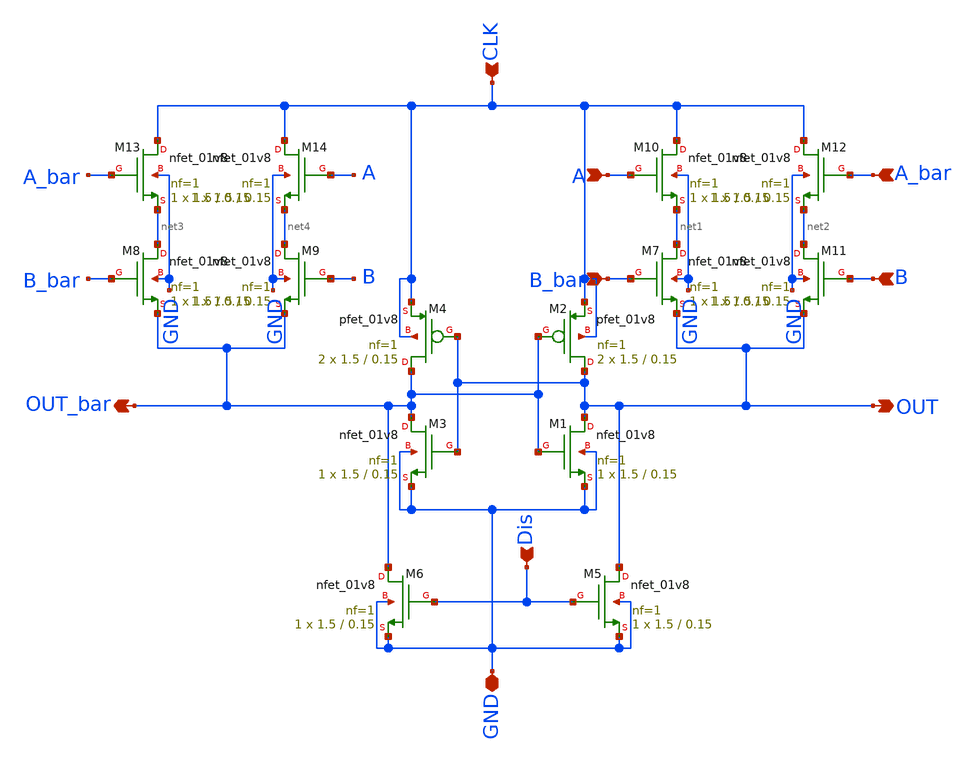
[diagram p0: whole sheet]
** sch_path: skywater_stuff/EESPFAL_XOR_v3_magic_checked.sch
**.subckt EESPFAL_XOR_v3_magic_checked A A_bar B B_bar OUT OUT_bar Dis GND CLK
*.ipin A
*.ipin A_bar
*.ipin B
*.ipin B_bar
*.opin OUT
*.opin OUT_bar
*.ipin Dis
*.iopin GND
*.ipin CLK
XM4 OUT_bar OUT CLK CLK sky130_fd_pr__pfet_01v8 L=0.15 W=1.5 nf=1 ad='int((nf+1)/2) * W/nf * 0.29' as='int((nf+2)/2) * W/nf * 0.29'
+ pd='2*int((nf+1)/2) * (W/nf + 0.29)' ps='2*int((nf+2)/2) * (W/nf + 0.29)' nrd='0.29 / W' nrs='0.29 / W'
+ sa=0 sb=0 sd=0 mult=2 m=2
XM3 OUT_bar OUT GND GND sky130_fd_pr__nfet_01v8 L=0.15 W=1.5 nf=1 ad='int((nf+1)/2) * W/nf * 0.29' as='int((nf+2)/2) * W/nf * 0.29'
+ pd='2*int((nf+1)/2) * (W/nf + 0.29)' ps='2*int((nf+2)/2) * (W/nf + 0.29)' nrd='0.29 / W' nrs='0.29 / W'
+ sa=0 sb=0 sd=0 mult=1 m=1
XM2 OUT OUT_bar CLK CLK sky130_fd_pr__pfet_01v8 L=0.15 W=1.5 nf=1 ad='int((nf+1)/2) * W/nf * 0.29' as='int((nf+2)/2) * W/nf * 0.29'
+ pd='2*int((nf+1)/2) * (W/nf + 0.29)' ps='2*int((nf+2)/2) * (W/nf + 0.29)' nrd='0.29 / W' nrs='0.29 / W'
+ sa=0 sb=0 sd=0 mult=2 m=2
XM11 net2 B OUT GND sky130_fd_pr__nfet_01v8 L=0.15 W=1.5 nf=1 ad='int((nf+1)/2) * W/nf * 0.29' as='int((nf+2)/2) * W/nf * 0.29'
+ pd='2*int((nf+1)/2) * (W/nf + 0.29)' ps='2*int((nf+2)/2) * (W/nf + 0.29)' nrd='0.29 / W' nrs='0.29 / W'
+ sa=0 sb=0 sd=0 mult=1 m=1
XM10 CLK A net1 GND sky130_fd_pr__nfet_01v8 L=0.15 W=1.5 nf=1 ad='int((nf+1)/2) * W/nf * 0.29' as='int((nf+2)/2) * W/nf * 0.29'
+ pd='2*int((nf+1)/2) * (W/nf + 0.29)' ps='2*int((nf+2)/2) * (W/nf + 0.29)' nrd='0.29 / W' nrs='0.29 / W'
+ sa=0 sb=0 sd=0 mult=1 m=1
XM12 CLK A_bar net2 GND sky130_fd_pr__nfet_01v8 L=0.15 W=1.5 nf=1 ad='int((nf+1)/2) * W/nf * 0.29' as='int((nf+2)/2) * W/nf * 0.29'
+ pd='2*int((nf+1)/2) * (W/nf + 0.29)' ps='2*int((nf+2)/2) * (W/nf + 0.29)' nrd='0.29 / W' nrs='0.29 / W'
+ sa=0 sb=0 sd=0 mult=1 m=1
XM8 net3 B_bar OUT_bar GND sky130_fd_pr__nfet_01v8 L=0.15 W=1.5 nf=1 ad='int((nf+1)/2) * W/nf * 0.29'
+ as='int((nf+2)/2) * W/nf * 0.29' pd='2*int((nf+1)/2) * (W/nf + 0.29)' ps='2*int((nf+2)/2) * (W/nf + 0.29)'
+ nrd='0.29 / W' nrs='0.29 / W' sa=0 sb=0 sd=0 mult=1 m=1
XM9 net4 B OUT_bar GND sky130_fd_pr__nfet_01v8 L=0.15 W=1.5 nf=1 ad='int((nf+1)/2) * W/nf * 0.29' as='int((nf+2)/2) * W/nf * 0.29'
+ pd='2*int((nf+1)/2) * (W/nf + 0.29)' ps='2*int((nf+2)/2) * (W/nf + 0.29)' nrd='0.29 / W' nrs='0.29 / W'
+ sa=0 sb=0 sd=0 mult=1 m=1
XM13 CLK A_bar net3 GND sky130_fd_pr__nfet_01v8 L=0.15 W=1.5 nf=1 ad='int((nf+1)/2) * W/nf * 0.29' as='int((nf+2)/2) * W/nf * 0.29'
+ pd='2*int((nf+1)/2) * (W/nf + 0.29)' ps='2*int((nf+2)/2) * (W/nf + 0.29)' nrd='0.29 / W' nrs='0.29 / W'
+ sa=0 sb=0 sd=0 mult=1 m=1
XM14 CLK A net4 GND sky130_fd_pr__nfet_01v8 L=0.15 W=1.5 nf=1 ad='int((nf+1)/2) * W/nf * 0.29' as='int((nf+2)/2) * W/nf * 0.29'
+ pd='2*int((nf+1)/2) * (W/nf + 0.29)' ps='2*int((nf+2)/2) * (W/nf + 0.29)' nrd='0.29 / W' nrs='0.29 / W'
+ sa=0 sb=0 sd=0 mult=1 m=1
XM7 net1 B_bar OUT GND sky130_fd_pr__nfet_01v8 L=0.15 W=1.5 nf=1 ad='int((nf+1)/2) * W/nf * 0.29' as='int((nf+2)/2) * W/nf * 0.29'
+ pd='2*int((nf+1)/2) * (W/nf + 0.29)' ps='2*int((nf+2)/2) * (W/nf + 0.29)' nrd='0.29 / W' nrs='0.29 / W'
+ sa=0 sb=0 sd=0 mult=1 m=1
XM1 OUT OUT_bar GND GND sky130_fd_pr__nfet_01v8 L=0.15 W=1.5 nf=1 ad='int((nf+1)/2) * W/nf * 0.29' as='int((nf+2)/2) * W/nf * 0.29'
+ pd='2*int((nf+1)/2) * (W/nf + 0.29)' ps='2*int((nf+2)/2) * (W/nf + 0.29)' nrd='0.29 / W' nrs='0.29 / W'
+ sa=0 sb=0 sd=0 mult=1 m=1
XM6 OUT_bar Dis GND GND sky130_fd_pr__nfet_01v8 L=0.15 W=1.5 nf=1 ad='int((nf+1)/2) * W/nf * 0.29' as='int((nf+2)/2) * W/nf * 0.29'
+ pd='2*int((nf+1)/2) * (W/nf + 0.29)' ps='2*int((nf+2)/2) * (W/nf + 0.29)' nrd='0.29 / W' nrs='0.29 / W'
+ sa=0 sb=0 sd=0 mult=1 m=1
XM5 OUT Dis GND GND sky130_fd_pr__nfet_01v8 L=0.15 W=1.5 nf=1 ad='int((nf+1)/2) * W/nf * 0.29' as='int((nf+2)/2) * W/nf * 0.29'
+ pd='2*int((nf+1)/2) * (W/nf + 0.29)' ps='2*int((nf+2)/2) * (W/nf + 0.29)' nrd='0.29 / W' nrs='0.29 / W'
+ sa=0 sb=0 sd=0 mult=1 m=1
**.ends
.end
